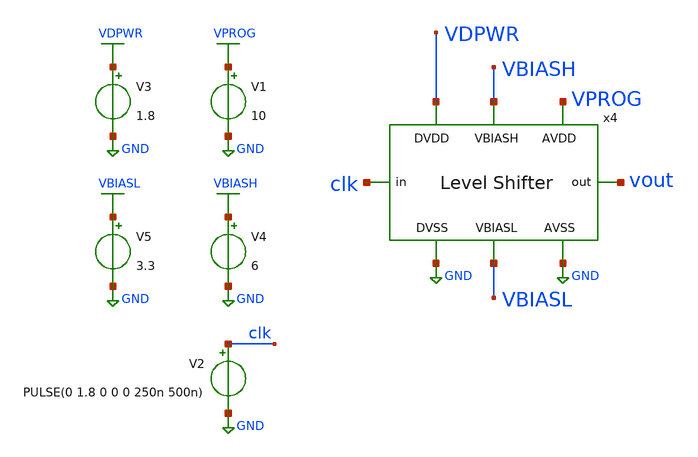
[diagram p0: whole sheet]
** sch_path: xschem/level_shifter_tb.sch
**.subckt level_shifter_tb
V1 VPROG GND 10
V2 clk GND PULSE(0 1.8 0 0 0 250n 500n)
V3 VDPWR GND 1.8
x4 VDPWR clk VBIASH vout VPROG GND GND VBIASL level_shifter
V4 VBIASH GND 6
V5 VBIASL GND 3.3
**** begin user architecture code

** opencircuitdesign pdks install
.lib $::SKYWATER_MODELS/sky130.lib.spice tt





.tran 10n 10u
.save all

.control
run
write level_shifter_tb.raw
.endc


**** end user architecture code
**.ends

* expanding   symbol:  level_shifter.sym # of pins=8
** sym_path: xschem/level_shifter.sym
** sch_path: xschem/level_shifter.sch
.subckt level_shifter DVDD in VBIASH out AVDD AVSS DVSS VBIASL
*.iopin AVDD
*.opin out
*.iopin AVSS
*.iopin DVDD
*.ipin in
*.iopin DVSS
*.iopin VBIASH
*.iopin VBIASL
XM1 in_b in DVSS DVSS sky130_fd_pr__nfet_01v8 L=3 W=1 nf=1 ad='int((nf+1)/2) * W/nf * 0.29' as='int((nf+2)/2) * W/nf * 0.29'
+ pd='2*int((nf+1)/2) * (W/nf + 0.29)' ps='2*int((nf+2)/2) * (W/nf + 0.29)' nrd='0.29 / W' nrs='0.29 / W'
+ sa=0 sb=0 sd=0 mult=1 m=1
XM2 in_b in DVDD DVDD sky130_fd_pr__pfet_01v8 L=3 W=1 nf=1 ad='int((nf+1)/2) * W/nf * 0.29' as='int((nf+2)/2) * W/nf * 0.29'
+ pd='2*int((nf+1)/2) * (W/nf + 0.29)' ps='2*int((nf+2)/2) * (W/nf + 0.29)' nrd='0.29 / W' nrs='0.29 / W'
+ sa=0 sb=0 sd=0 mult=1 m=1
XM3 high_1 high_2 AVDD AVDD sky130_fd_pr__pfet_g5v0d10v5 L=3 W=1 nf=1 ad='int((nf+1)/2) * W/nf * 0.29'
+ as='int((nf+2)/2) * W/nf * 0.29' pd='2*int((nf+1)/2) * (W/nf + 0.29)' ps='2*int((nf+2)/2) * (W/nf + 0.29)'
+ nrd='0.29 / W' nrs='0.29 / W' sa=0 sb=0 sd=0 mult=1 m=1
XM4 high_2 high_1 AVDD AVDD sky130_fd_pr__pfet_g5v0d10v5 L=3 W=1 nf=1 ad='int((nf+1)/2) * W/nf * 0.29'
+ as='int((nf+2)/2) * W/nf * 0.29' pd='2*int((nf+1)/2) * (W/nf + 0.29)' ps='2*int((nf+2)/2) * (W/nf + 0.29)'
+ nrd='0.29 / W' nrs='0.29 / W' sa=0 sb=0 sd=0 mult=1 m=1
XM8 low_2 in AVSS AVSS sky130_fd_pr__nfet_g5v0d10v5 L=3 W=2 nf=1 ad='int((nf+1)/2) * W/nf * 0.29' as='int((nf+2)/2) * W/nf * 0.29'
+ pd='2*int((nf+1)/2) * (W/nf + 0.29)' ps='2*int((nf+2)/2) * (W/nf + 0.29)' nrd='0.29 / W' nrs='0.29 / W'
+ sa=0 sb=0 sd=0 mult=1 m=1
XM7 low_1 in_b AVSS AVSS sky130_fd_pr__nfet_g5v0d10v5 L=3 W=2 nf=1 ad='int((nf+1)/2) * W/nf * 0.29' as='int((nf+2)/2) * W/nf * 0.29'
+ pd='2*int((nf+1)/2) * (W/nf + 0.29)' ps='2*int((nf+2)/2) * (W/nf + 0.29)' nrd='0.29 / W' nrs='0.29 / W'
+ sa=0 sb=0 sd=0 mult=1 m=1
XM5 mid_1 VBIASH high_1 high_1 sky130_fd_pr__pfet_g5v0d10v5 L=3 W=1 nf=1 ad='int((nf+1)/2) * W/nf * 0.29'
+ as='int((nf+2)/2) * W/nf * 0.29' pd='2*int((nf+1)/2) * (W/nf + 0.29)' ps='2*int((nf+2)/2) * (W/nf + 0.29)'
+ nrd='0.29 / W' nrs='0.29 / W' sa=0 sb=0 sd=0 mult=1 m=1
XM6 mid_2 VBIASH high_2 high_2 sky130_fd_pr__pfet_g5v0d10v5 L=3 W=1 nf=1 ad='int((nf+1)/2) * W/nf * 0.29'
+ as='int((nf+2)/2) * W/nf * 0.29' pd='2*int((nf+1)/2) * (W/nf + 0.29)' ps='2*int((nf+2)/2) * (W/nf + 0.29)'
+ nrd='0.29 / W' nrs='0.29 / W' sa=0 sb=0 sd=0 mult=1 m=1
XM9 mid_2 VBIASL low_2 low_2 sky130_fd_pr__nfet_g5v0d10v5 L=3 W=2 nf=1 ad='int((nf+1)/2) * W/nf * 0.29'
+ as='int((nf+2)/2) * W/nf * 0.29' pd='2*int((nf+1)/2) * (W/nf + 0.29)' ps='2*int((nf+2)/2) * (W/nf + 0.29)'
+ nrd='0.29 / W' nrs='0.29 / W' sa=0 sb=0 sd=0 mult=1 m=1
XM10 mid_1 VBIASL low_1 low_1 sky130_fd_pr__nfet_g5v0d10v5 L=3 W=2 nf=1 ad='int((nf+1)/2) * W/nf * 0.29'
+ as='int((nf+2)/2) * W/nf * 0.29' pd='2*int((nf+1)/2) * (W/nf + 0.29)' ps='2*int((nf+2)/2) * (W/nf + 0.29)'
+ nrd='0.29 / W' nrs='0.29 / W' sa=0 sb=0 sd=0 mult=1 m=1
XM11 out low_2 AVSS AVSS sky130_fd_pr__nfet_g5v0d10v5 L=3 W=2 nf=1 ad='int((nf+1)/2) * W/nf * 0.29' as='int((nf+2)/2) * W/nf * 0.29'
+ pd='2*int((nf+1)/2) * (W/nf + 0.29)' ps='2*int((nf+2)/2) * (W/nf + 0.29)' nrd='0.29 / W' nrs='0.29 / W'
+ sa=0 sb=0 sd=0 mult=1 m=1
XM12 out high_2 AVDD AVDD sky130_fd_pr__pfet_g5v0d10v5 L=3 W=1 nf=1 ad='int((nf+1)/2) * W/nf * 0.29'
+ as='int((nf+2)/2) * W/nf * 0.29' pd='2*int((nf+1)/2) * (W/nf + 0.29)' ps='2*int((nf+2)/2) * (W/nf + 0.29)'
+ nrd='0.29 / W' nrs='0.29 / W' sa=0 sb=0 sd=0 mult=1 m=1
.ends

.GLOBAL GND
.GLOBAL VPROG
.GLOBAL VDPWR
.GLOBAL VBIASH
.GLOBAL VBIASL
.end
